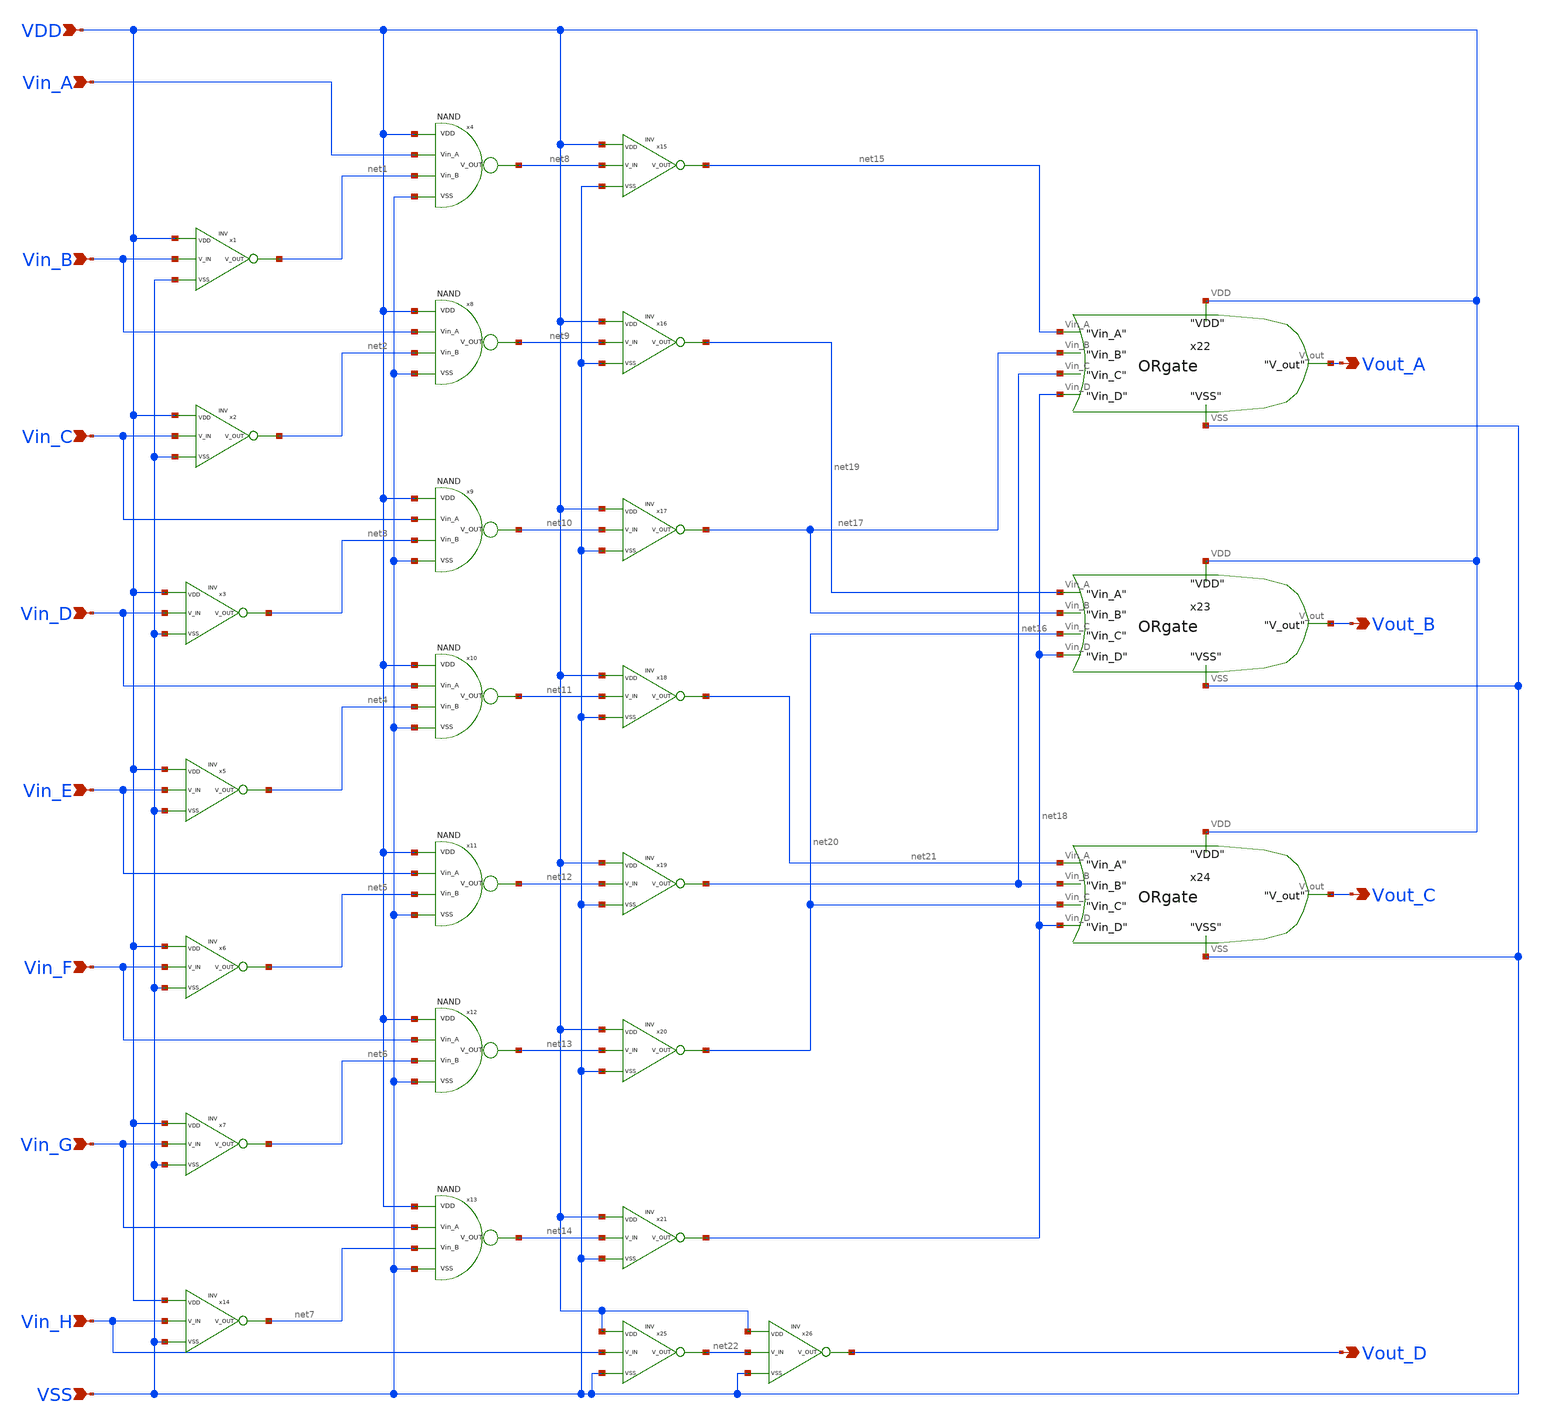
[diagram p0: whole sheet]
** sch_path: schematics_xschem/8to4Encoder.sch
**.subckt 8to4Encoder Vin_C Vin_D Vin_A Vin_B Vin_E Vin_F Vin_H VDD Vin_G VSS Vout_D Vout_C Vout_B
*+ Vout_A
*.ipin Vin_C
*.ipin Vin_D
*.ipin Vin_A
*.ipin Vin_B
*.ipin Vin_E
*.ipin Vin_F
*.ipin Vin_H
*.ipin VDD
*.ipin Vin_G
*.ipin VSS
*.opin Vout_D
*.opin Vout_C
*.opin Vout_B
*.opin Vout_A
x4 VDD Vin_A net8 net1 VSS NAND
x1 VDD Vin_B net1 VSS INV
x2 VDD Vin_C net2 VSS INV
x3 VDD Vin_D net3 VSS INV
x5 VDD Vin_E net4 VSS INV
x6 VDD Vin_F net5 VSS INV
x7 VDD Vin_G net6 VSS INV
x8 VDD Vin_B net9 net2 VSS NAND
x9 VDD Vin_C net10 net3 VSS NAND
x10 VDD Vin_D net11 net4 VSS NAND
x11 VDD Vin_E net12 net5 VSS NAND
x12 VDD Vin_F net13 net6 VSS NAND
x13 VDD Vin_G net14 net7 VSS NAND
x14 VDD Vin_H net7 VSS INV
x15 VDD net8 net15 VSS INV
x16 VDD net9 net19 VSS INV
x17 VDD net10 net17 VSS INV
x18 VDD net11 net21 VSS INV
x19 VDD net12 net16 VSS INV
x20 VDD net13 net20 VSS INV
x21 VDD net14 net18 VSS INV
x22 VDD net15 net17 net16 net18 Vout_A VSS ORgate
x23 VDD net19 net17 net20 net18 Vout_B VSS ORgate
x24 VDD net21 net16 net20 net18 Vout_C VSS ORgate
x25 VDD Vin_H net22 VSS INV
x26 VDD net22 Vout_D VSS INV
**.ends

* expanding   symbol:  NAND.sym # of pins=5
** sym_path: schematics_xschem/NAND.sym
** sch_path: schematics_xschem/NAND.sch
.subckt NAND VDD Vin_A V_OUT Vin_B VSS
*.ipin Vin_A
*.opin V_OUT
*.ipin Vin_B
*.ipin VSS
*.ipin VDD
XM1 V_OUT Vin_A VDD VDD sky130_fd_pr__pfet_01v8 L=0.15 W=1 nf=1 ad='int((nf+1)/2) * W/nf * 0.29' as='int((nf+2)/2) * W/nf * 0.29'
+ pd='2*int((nf+1)/2) * (W/nf + 0.29)' ps='2*int((nf+2)/2) * (W/nf + 0.29)' nrd='0.29 / W' nrs='0.29 / W'
+ sa=0 sb=0 sd=0 mult=1 m=1
XM2 V_OUT Vin_A net1 VSS sky130_fd_pr__nfet_01v8 L=0.15 W=1 nf=1 ad='int((nf+1)/2) * W/nf * 0.29' as='int((nf+2)/2) * W/nf * 0.29'
+ pd='2*int((nf+1)/2) * (W/nf + 0.29)' ps='2*int((nf+2)/2) * (W/nf + 0.29)' nrd='0.29 / W' nrs='0.29 / W'
+ sa=0 sb=0 sd=0 mult=1 m=1
XM3 V_OUT Vin_B VDD VDD sky130_fd_pr__pfet_01v8 L=0.15 W=1 nf=1 ad='int((nf+1)/2) * W/nf * 0.29' as='int((nf+2)/2) * W/nf * 0.29'
+ pd='2*int((nf+1)/2) * (W/nf + 0.29)' ps='2*int((nf+2)/2) * (W/nf + 0.29)' nrd='0.29 / W' nrs='0.29 / W'
+ sa=0 sb=0 sd=0 mult=1 m=1
XM4 net1 Vin_B VSS VSS sky130_fd_pr__nfet_01v8 L=0.15 W=1 nf=1 ad='int((nf+1)/2) * W/nf * 0.29' as='int((nf+2)/2) * W/nf * 0.29'
+ pd='2*int((nf+1)/2) * (W/nf + 0.29)' ps='2*int((nf+2)/2) * (W/nf + 0.29)' nrd='0.29 / W' nrs='0.29 / W'
+ sa=0 sb=0 sd=0 mult=1 m=1
.ends


* expanding   symbol:  INV.sym # of pins=4
** sym_path: schematics_xschem/INV.sym
** sch_path: schematics_xschem/INV.sch
.subckt INV VDD V_IN V_OUT VSS
*.ipin V_IN
*.opin V_OUT
*.ipin VDD
*.ipin VSS
XM1 V_OUT V_IN VSS VSS sky130_fd_pr__nfet_01v8 L=0.15 W=1 nf=1 ad='int((nf+1)/2) * W/nf * 0.29' as='int((nf+2)/2) * W/nf * 0.29'
+ pd='2*int((nf+1)/2) * (W/nf + 0.29)' ps='2*int((nf+2)/2) * (W/nf + 0.29)' nrd='0.29 / W' nrs='0.29 / W'
+ sa=0 sb=0 sd=0 mult=1 m=1
Xx2 V_OUT V_IN VDD VDD sky130_fd_pr__pfet_01v8 L=0.15 W=1 nf=1 ad='int((nf+1)/2) * W/nf * 0.29' as='int((nf+2)/2) * W/nf * 0.29'
+ pd='2*int((nf+1)/2) * (W/nf + 0.29)' ps='2*int((nf+2)/2) * (W/nf + 0.29)' nrd='0.29 / W' nrs='0.29 / W'
+ sa=0 sb=0 sd=0 mult=1 m=1
.ends


* expanding   symbol:  ORgate.sym # of pins=7
** sym_path: schematics_xschem/ORgate.sym
** sch_path: schematics_xschem/ORgate.sch
.subckt ORgate VDD Vin_A Vin_B Vin_C Vin_D V_out VSS
*.ipin Vin_A
*.ipin Vin_B
*.ipin Vin_C
*.ipin Vin_D
*.opin V_out
*.ipin VSS
*.ipin VDD
XM5 net4 Vin_D VSS VSS sky130_fd_pr__nfet_01v8 L=0.15 W=1 nf=1 ad='int((nf+1)/2) * W/nf * 0.29' as='int((nf+2)/2) * W/nf * 0.29'
+ pd='2*int((nf+1)/2) * (W/nf + 0.29)' ps='2*int((nf+2)/2) * (W/nf + 0.29)' nrd='0.29 / W' nrs='0.29 / W'
+ sa=0 sb=0 sd=0 mult=1 m=1
XM7 net4 Vin_C VSS VSS sky130_fd_pr__nfet_01v8 L=0.15 W=1 nf=1 ad='int((nf+1)/2) * W/nf * 0.29' as='int((nf+2)/2) * W/nf * 0.29'
+ pd='2*int((nf+1)/2) * (W/nf + 0.29)' ps='2*int((nf+2)/2) * (W/nf + 0.29)' nrd='0.29 / W' nrs='0.29 / W'
+ sa=0 sb=0 sd=0 mult=1 m=1
XM8 net4 Vin_B VSS VSS sky130_fd_pr__nfet_01v8 L=0.15 W=1 nf=1 ad='int((nf+1)/2) * W/nf * 0.29' as='int((nf+2)/2) * W/nf * 0.29'
+ pd='2*int((nf+1)/2) * (W/nf + 0.29)' ps='2*int((nf+2)/2) * (W/nf + 0.29)' nrd='0.29 / W' nrs='0.29 / W'
+ sa=0 sb=0 sd=0 mult=1 m=1
XM10 net4 Vin_A VSS VSS sky130_fd_pr__nfet_01v8 L=0.15 W=1 nf=1 ad='int((nf+1)/2) * W/nf * 0.29' as='int((nf+2)/2) * W/nf * 0.29'
+ pd='2*int((nf+1)/2) * (W/nf + 0.29)' ps='2*int((nf+2)/2) * (W/nf + 0.29)' nrd='0.29 / W' nrs='0.29 / W'
+ sa=0 sb=0 sd=0 mult=1 m=1
XM11 net3 Vin_A VDD VDD sky130_fd_pr__pfet_01v8 L=0.15 W=1 nf=1 ad='int((nf+1)/2) * W/nf * 0.29' as='int((nf+2)/2) * W/nf * 0.29'
+ pd='2*int((nf+1)/2) * (W/nf + 0.29)' ps='2*int((nf+2)/2) * (W/nf + 0.29)' nrd='0.29 / W' nrs='0.29 / W'
+ sa=0 sb=0 sd=0 mult=1 m=1
XM1 net2 Vin_B net3 VDD sky130_fd_pr__pfet_01v8 L=0.15 W=1 nf=1 ad='int((nf+1)/2) * W/nf * 0.29' as='int((nf+2)/2) * W/nf * 0.29'
+ pd='2*int((nf+1)/2) * (W/nf + 0.29)' ps='2*int((nf+2)/2) * (W/nf + 0.29)' nrd='0.29 / W' nrs='0.29 / W'
+ sa=0 sb=0 sd=0 mult=1 m=1
XM2 net1 Vin_C net2 VDD sky130_fd_pr__pfet_01v8 L=0.15 W=1 nf=1 ad='int((nf+1)/2) * W/nf * 0.29' as='int((nf+2)/2) * W/nf * 0.29'
+ pd='2*int((nf+1)/2) * (W/nf + 0.29)' ps='2*int((nf+2)/2) * (W/nf + 0.29)' nrd='0.29 / W' nrs='0.29 / W'
+ sa=0 sb=0 sd=0 mult=1 m=1
XM3 net4 Vin_D net1 VDD sky130_fd_pr__pfet_01v8 L=0.15 W=1 nf=1 ad='int((nf+1)/2) * W/nf * 0.29' as='int((nf+2)/2) * W/nf * 0.29'
+ pd='2*int((nf+1)/2) * (W/nf + 0.29)' ps='2*int((nf+2)/2) * (W/nf + 0.29)' nrd='0.29 / W' nrs='0.29 / W'
+ sa=0 sb=0 sd=0 mult=1 m=1
.ends

.end
